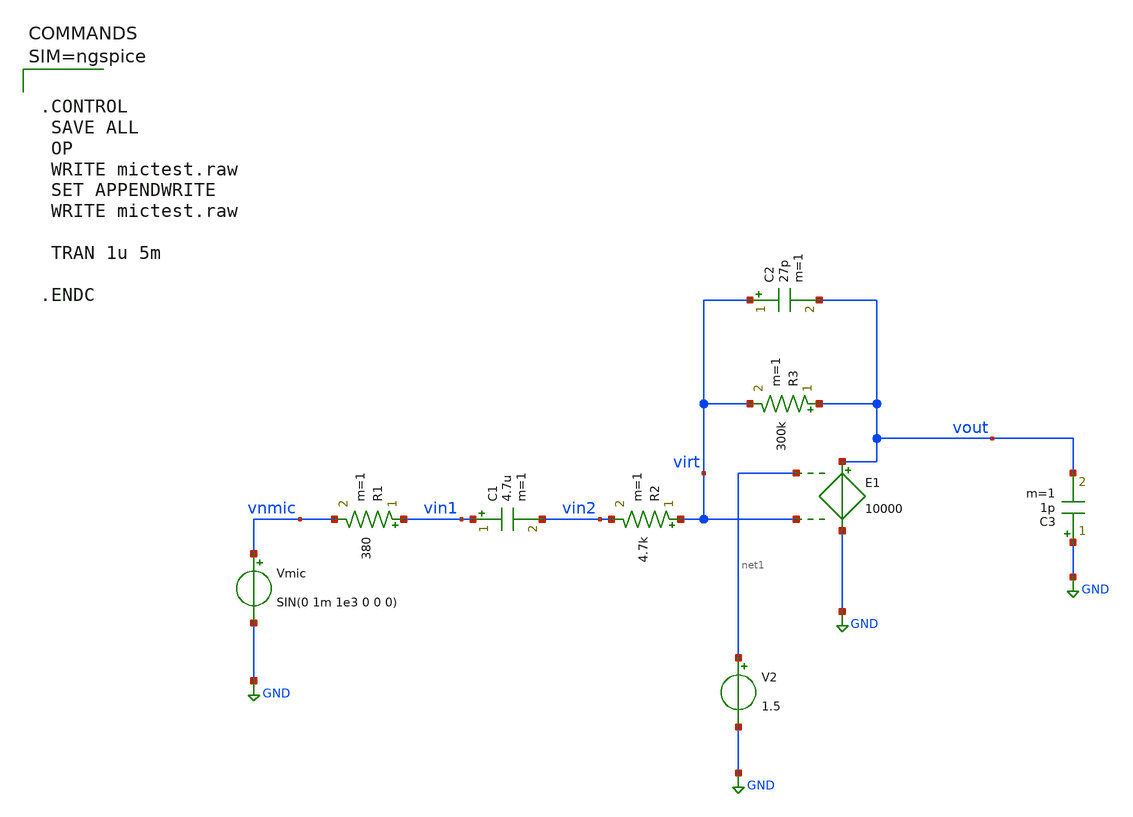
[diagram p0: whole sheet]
** sch_path: xschem/mictest_transient.sch
**.subckt mictest_transient
Vmic vnmic GND SIN(0 1m 1e3 0 0 0)
R1 vin1 vnmic 380 m=1
C1 vin1 vin2 4.7u m=1
R2 virt vin2 4.7k m=1
R3 vout virt 300k m=1
C2 virt vout 27p m=1
V2 net1 GND 1.5
C3 GND vout 1p m=1
E1 vout GND net1 virt 10000
**** begin user architecture code



.CONTROL
 SAVE ALL
 OP
 WRITE mictest.raw
 SET APPENDWRITE
 WRITE mictest.raw

 TRAN 1u 5m

.ENDC



**** end user architecture code
**.ends
.GLOBAL GND
.end
